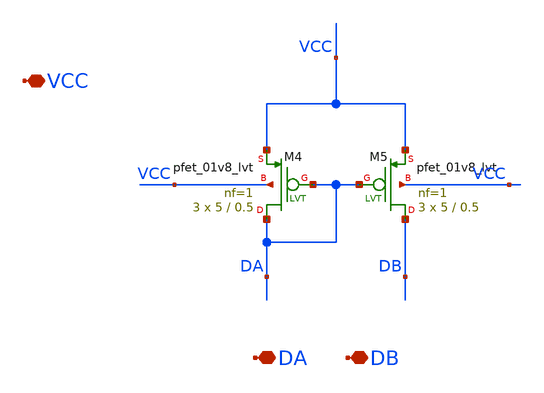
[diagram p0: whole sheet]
** sch_path: xschem/activeload.sch
**.subckt activeload DA DB VCC
*.iopin DA
*.iopin DB
*.iopin VCC
XM4 DA DA VCC VCC sky130_fd_pr__pfet_01v8_lvt L=0.5 W=5 nf=1 ad='int((nf+1)/2) * W/nf * 0.29' as='int((nf+2)/2) * W/nf * 0.29'
+ pd='2*int((nf+1)/2) * (W/nf + 0.29)' ps='2*int((nf+2)/2) * (W/nf + 0.29)' nrd='0.29 / W' nrs='0.29 / W'
+ sa=0 sb=0 sd=0 mult=3 m=3
XM5 DB DA VCC VCC sky130_fd_pr__pfet_01v8_lvt L=0.5 W=5 nf=1 ad='int((nf+1)/2) * W/nf * 0.29' as='int((nf+2)/2) * W/nf * 0.29'
+ pd='2*int((nf+1)/2) * (W/nf + 0.29)' ps='2*int((nf+2)/2) * (W/nf + 0.29)' nrd='0.29 / W' nrs='0.29 / W'
+ sa=0 sb=0 sd=0 mult=3 m=3
**.ends
.end
